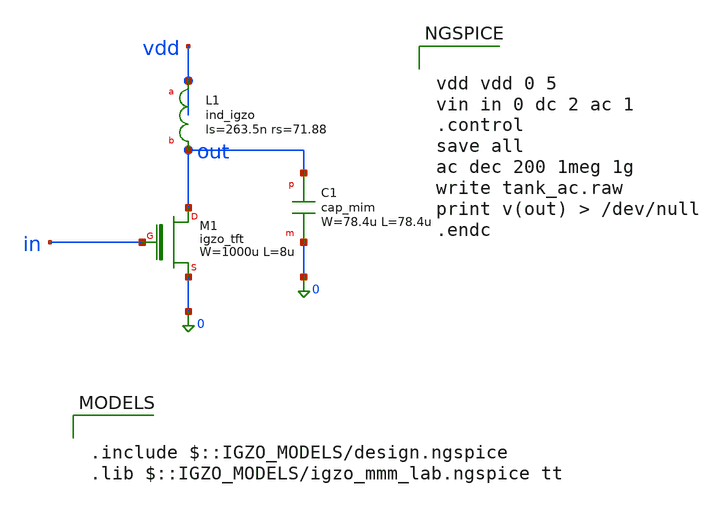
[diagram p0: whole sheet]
** sch_path: libs.tech/xschem/tests/tank_ac.sch
**.subckt tank_ac
XM1 out in 0 igzo_tft W=1000u L=8u ov=5u nf=1 m=1
XL1 vdd out ind_igzo ls=263.5n rs=71.88
XC1 out 0 cap_mim W=78.4u L=78.4u
**** begin user architecture code

.include $::IGZO_MODELS/design.ngspice
.lib $::IGZO_MODELS/igzo_mmm_lab.ngspice tt



vdd vdd 0 5
vin in 0 dc 2 ac 1
.control
save all
ac dec 200 1meg 1g
write tank_ac.raw
print v(out) > /dev/null
.endc


**** end user architecture code
**.ends
.end
